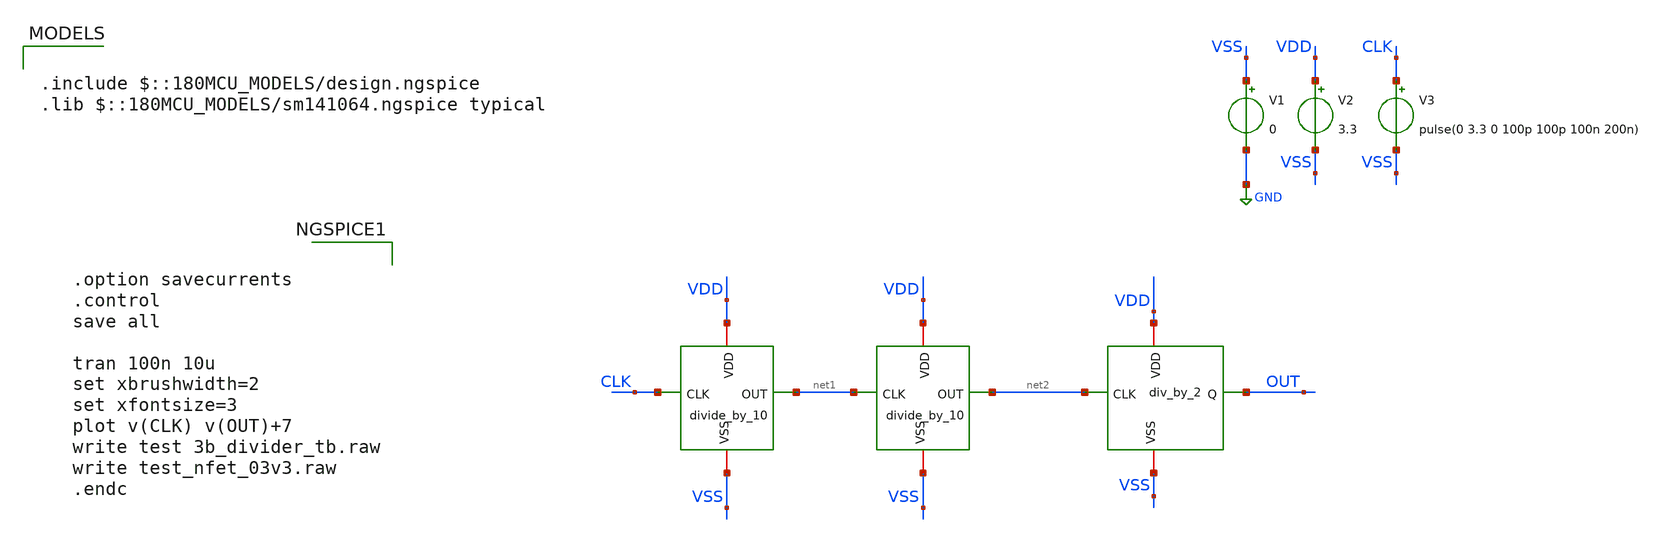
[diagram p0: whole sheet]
** sch_path: Clock_Generator_PAKISTAN_06/Schematics/div_by_100.sch
**.subckt div_by_100
x1 VDD net1 CLK VSS divide_by_10
x2 VDD net2 net1 VSS divide_by_10
x3 net2 VDD OUT VSS div_by_2
V1 VSS GND 0
V2 VDD VSS 3.3
V3 CLK VSS pulse(0 3.3 0 100p 100p 100n 200n)
**** begin user architecture code

.include $::180MCU_MODELS/design.ngspice
.lib $::180MCU_MODELS/sm141064.ngspice typical



.option savecurrents
.control
save all

tran 100n 10u
set xbrushwidth=2
set xfontsize=3
plot v(CLK) v(OUT)+7
write test 3b_divider_tb.raw
write test_nfet_03v3.raw
.endc


**** end user architecture code
**.ends
.GLOBAL GND
.end
